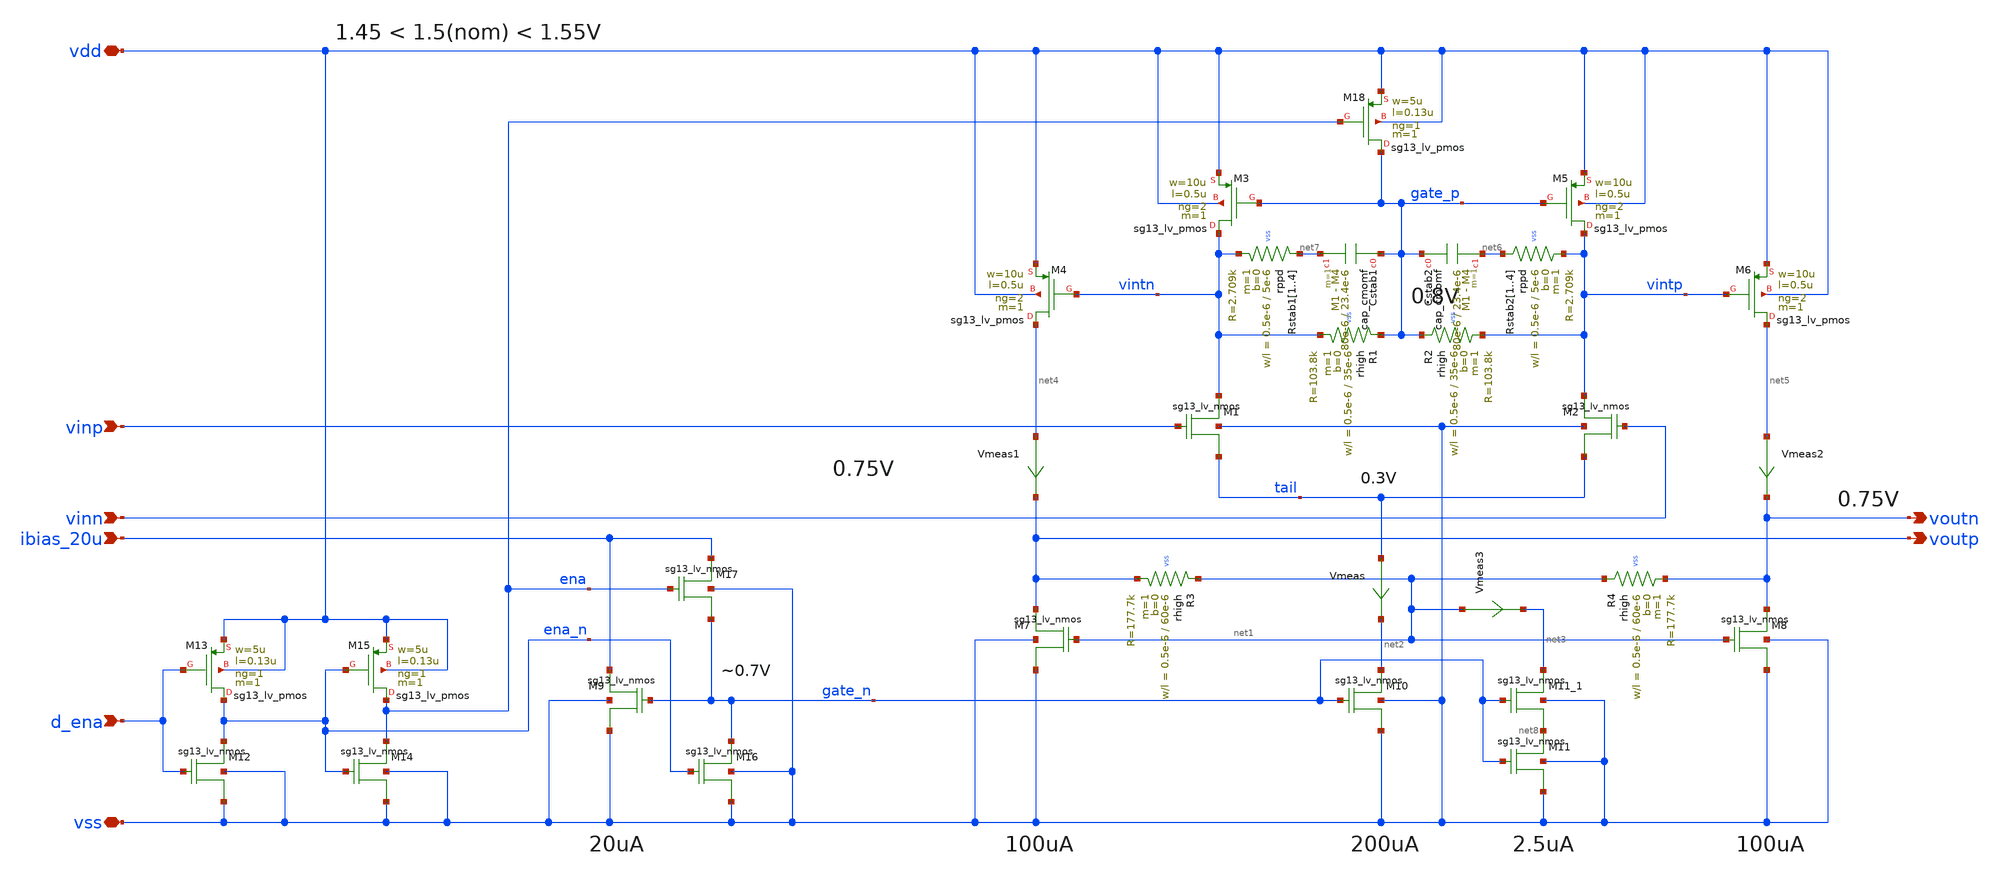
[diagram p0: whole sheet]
** sch_path: xschem/ota-diff.sch
* (c) 2025 Harald Pretl, Apache-2.0 license
**.subckt ota-diff ibias_20u vdd vss vinp vinn voutp d_ena voutn
*.ipin ibias_20u
*.iopin vdd
*.iopin vss
*.ipin vinp
*.ipin vinn
*.opin voutp
*.ipin d_ena
*.opin voutn
XM10 net2 gate_n vss vss sg13_lv_nmos w=200u l=5u ng=40 m=1
XM1 vintn vinp tail vss sg13_lv_nmos w=10u l=0.5u ng=2 m=1
XM2 vintp vinn tail vss sg13_lv_nmos w=10u l=0.5u ng=2 m=1
XM3 vintn gate_p vdd vdd sg13_lv_pmos w=10u l=0.5u ng=2 m=1 mm_ok=1
XM9 ibias_20u gate_n vss vss sg13_lv_nmos w=20u l=5u ng=4 m=1
XM16 gate_n ena_n vss vss sg13_lv_nmos w=5u l=0.13u ng=1 m=1
XM18 gate_p ena vdd vdd sg13_lv_pmos w=5u l=0.13u ng=1 m=1 mm_ok=1
XM14 ena ena_n vss vss sg13_lv_nmos w=5u l=0.13u ng=1 m=1
XM15 ena ena_n vdd vdd sg13_lv_pmos w=5u l=0.13u ng=1 m=1 mm_ok=1
XM17 ibias_20u ena gate_n vss sg13_lv_nmos w=5u l=0.13u ng=1 m=1
XM12 ena_n d_ena vss vss sg13_lv_nmos w=5u l=0.13u ng=1 m=1
XM13 ena_n d_ena vdd vdd sg13_lv_pmos w=5u l=0.13u ng=1 m=1 mm_ok=1
XM7 voutp net1 vss vss sg13_lv_nmos w=20u l=5u ng=4 m=1
XR1 gate_p vintn VSS rhigh w=0.5e-6 l=35e-6 m=1 b=0 mm_ok=1
XR3 net1 voutp VSS rhigh w=0.5e-6 l=60e-6 m=1 b=0 mm_ok=1
XM11_1 net3 gate_n net8 vss sg13_lv_nmos w=5u l=5u ng=1 m=1
XM5 vintp gate_p vdd vdd sg13_lv_pmos w=10u l=0.5u ng=2 m=1 mm_ok=1
XM4 net4 vintn vdd vdd sg13_lv_pmos w=10u l=0.5u ng=2 m=1 mm_ok=1
XM6 net5 vintp vdd vdd sg13_lv_pmos w=10u l=0.5u ng=2 m=1 mm_ok=1
XR2 gate_p vintp VSS rhigh w=0.5e-6 l=35e-6 m=1 b=0 mm_ok=1
XM8 voutn net1 vss vss sg13_lv_nmos w=20u l=5u ng=4 m=1
XR4 net1 voutn VSS rhigh w=0.5e-6 l=60e-6 m=1 b=0 mm_ok=1
Vmeas tail net2 0
.save i(vmeas)
Vmeas1 net4 voutp 0
.save i(vmeas1)
Vmeas2 net5 voutn 0
.save i(vmeas2)
Vmeas3 net1 net3 0
.save i(vmeas3)
XCstab1 gate_p net7 cap_cmomf w=80e-6 l=23.4e-6 mmin=1 mmax=4 subblock=0 rfmodel=0 subscale=1 m=1
+ mm_ok=1
XCstab2 gate_p net6 cap_cmomf w=80e-6 l=23.4e-6 mmin=1 mmax=4 subblock=0 rfmodel=0 subscale=1 m=1
+ mm_ok=1
XRstab11 net7 vintn VSS rppd w=0.5e-6 l=5e-6 m=1 b=0 mm_ok=1
XRstab12 net7 vintn VSS rppd w=0.5e-6 l=5e-6 m=1 b=0 mm_ok=1
XRstab13 net7 vintn VSS rppd w=0.5e-6 l=5e-6 m=1 b=0 mm_ok=1
XRstab14 net7 vintn VSS rppd w=0.5e-6 l=5e-6 m=1 b=0 mm_ok=1
XRstab21 net6 vintp VSS rppd w=0.5e-6 l=5e-6 m=1 b=0 mm_ok=1
XRstab22 net6 vintp VSS rppd w=0.5e-6 l=5e-6 m=1 b=0 mm_ok=1
XRstab23 net6 vintp VSS rppd w=0.5e-6 l=5e-6 m=1 b=0 mm_ok=1
XRstab24 net6 vintp VSS rppd w=0.5e-6 l=5e-6 m=1 b=0 mm_ok=1
XM11 net8 gate_n vss vss sg13_lv_nmos w=5u l=5u ng=1 m=1
**.ends
.end
